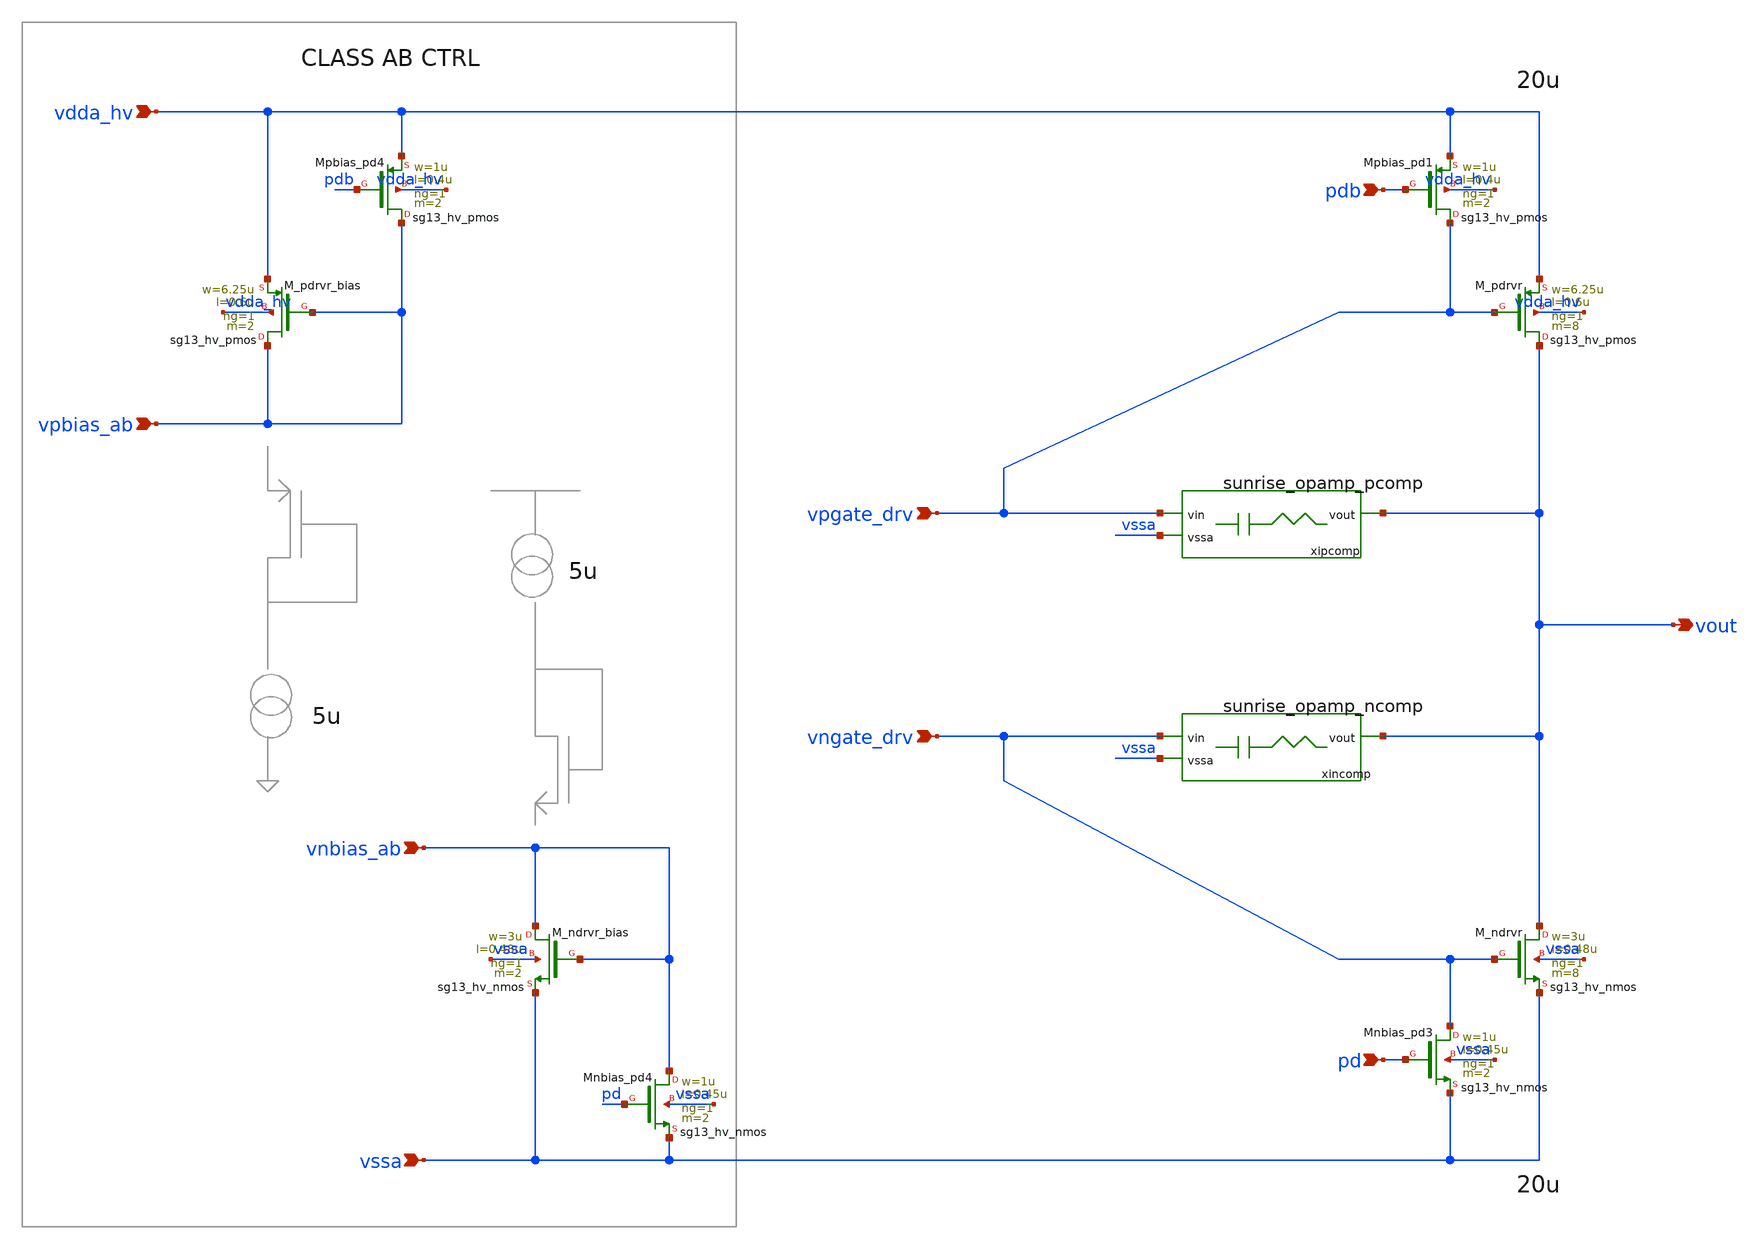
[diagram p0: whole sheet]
** sch_path: Schematics_Layout/sunrise_opamp_stg2/sunrise_opamp_stg2.sch
**.subckt sunrise_opamp_stg2 vdda_hv vssa vpgate_drv vngate_drv pd pdb vout vnbias_ab vpbias_ab
*.ipin vdda_hv
*.ipin vssa
*.ipin vpgate_drv
*.ipin vngate_drv
*.ipin pd
*.ipin pdb
*.opin vout
*.ipin vnbias_ab
*.ipin vpbias_ab
XM_ndrvr vout vngate_drv vssa vssa sg13_hv_nmos w=3u l=0.48u ng=1 m=8 mm_ok=1
XM_pdrvr vout vpgate_drv vdda_hv vdda_hv sg13_hv_pmos w=6.25u l=0.6u ng=1 m=8 mm_ok=1
XMnbias_pd3 vngate_drv pd vssa vssa sg13_hv_nmos w=1u l=0.45u ng=1 m=2 mm_ok=1
XMpbias_pd1 vpgate_drv pdb vdda_hv vdda_hv sg13_hv_pmos w=1u l=0.4u ng=1 m=2 mm_ok=1
xipcomp vssa vout vpgate_drv sunrise_opamp_pcomp
xincomp vssa vout vngate_drv sunrise_opamp_ncomp
XM_pdrvr_bias vpbias_ab vpbias_ab vdda_hv vdda_hv sg13_hv_pmos w=6.25u l=0.6u ng=1 m=2 mm_ok=1
XM_ndrvr_bias vnbias_ab vnbias_ab vssa vssa sg13_hv_nmos w=3u l=0.48u ng=1 m=2 mm_ok=1
XMpbias_pd4 vpbias_ab pdb vdda_hv vdda_hv sg13_hv_pmos w=1u l=0.4u ng=1 m=2 mm_ok=1
XMnbias_pd4 vnbias_ab pd vssa vssa sg13_hv_nmos w=1u l=0.45u ng=1 m=2 mm_ok=1
**.ends
.end
